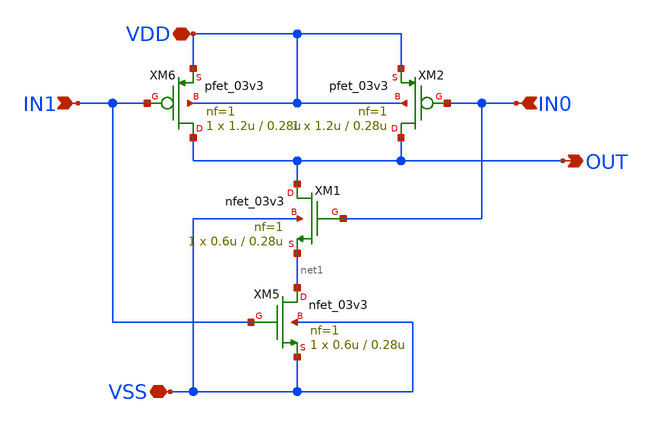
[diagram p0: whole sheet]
** sch_path: xschem/io_nand2_1.sch
* Copyright 2023 David Mitchell Bailey
* Licensed under the Apache License, Version 2.0 (the "License");
* you may not use this file except in compliance with the License.
* You may obtain a copy of the License at
* https://www.apache.org/licenses/LICENSE-2.0
* Unless required by applicable law or agreed to in writing, software
* distributed under the License is distributed on an "AS IS" BASIS,
* WITHOUT WARRANTIES OR CONDITIONS OF ANY KIND, either express or implied.
* See the License for the specific language governing permissions and
* limitations under the License.
**.subckt io_nand2_1 OUT IN0 IN1 VDD VSS
*.opin OUT
*.ipin IN0
*.ipin IN1
*.iopin VDD
*.iopin VSS
XM5 net1 IN1 VSS VSS nfet_03v3 L=0.28u W=0.6u nf=1 ad='int((nf+1)/2) * W/nf * 0.18u' as='int((nf+2)/2) * W/nf * 0.18u'
+ pd='2*int((nf+1)/2) * (W/nf + 0.18u)' ps='2*int((nf+2)/2) * (W/nf + 0.18u)' nrd='0.18u / W' nrs='0.18u / W'
+ sa=0 sb=0 sd=0 m=1 par=1
XM6 OUT IN1 VDD VDD pfet_03v3 L=0.28u W=1.2u nf=1 ad='int((nf+1)/2) * W/nf * 0.18u' as='int((nf+2)/2) * W/nf * 0.18u'
+ pd='2*int((nf+1)/2) * (W/nf + 0.18u)' ps='2*int((nf+2)/2) * (W/nf + 0.18u)' nrd='0.18u / W' nrs='0.18u / W'
+ sa=0 sb=0 sd=0 m=1 par=1
XM1 OUT IN0 net1 VSS nfet_03v3 L=0.28u W=0.6u nf=1 ad='int((nf+1)/2) * W/nf * 0.18u' as='int((nf+2)/2) * W/nf * 0.18u'
+ pd='2*int((nf+1)/2) * (W/nf + 0.18u)' ps='2*int((nf+2)/2) * (W/nf + 0.18u)' nrd='0.18u / W' nrs='0.18u / W'
+ sa=0 sb=0 sd=0 m=1 par=1
XM2 OUT IN0 VDD VDD pfet_03v3 L=0.28u W=1.2u nf=1 ad='int((nf+1)/2) * W/nf * 0.18u' as='int((nf+2)/2) * W/nf * 0.18u'
+ pd='2*int((nf+1)/2) * (W/nf + 0.18u)' ps='2*int((nf+2)/2) * (W/nf + 0.18u)' nrd='0.18u / W' nrs='0.18u / W'
+ sa=0 sb=0 sd=0 m=1 par=1
**.ends
.end
